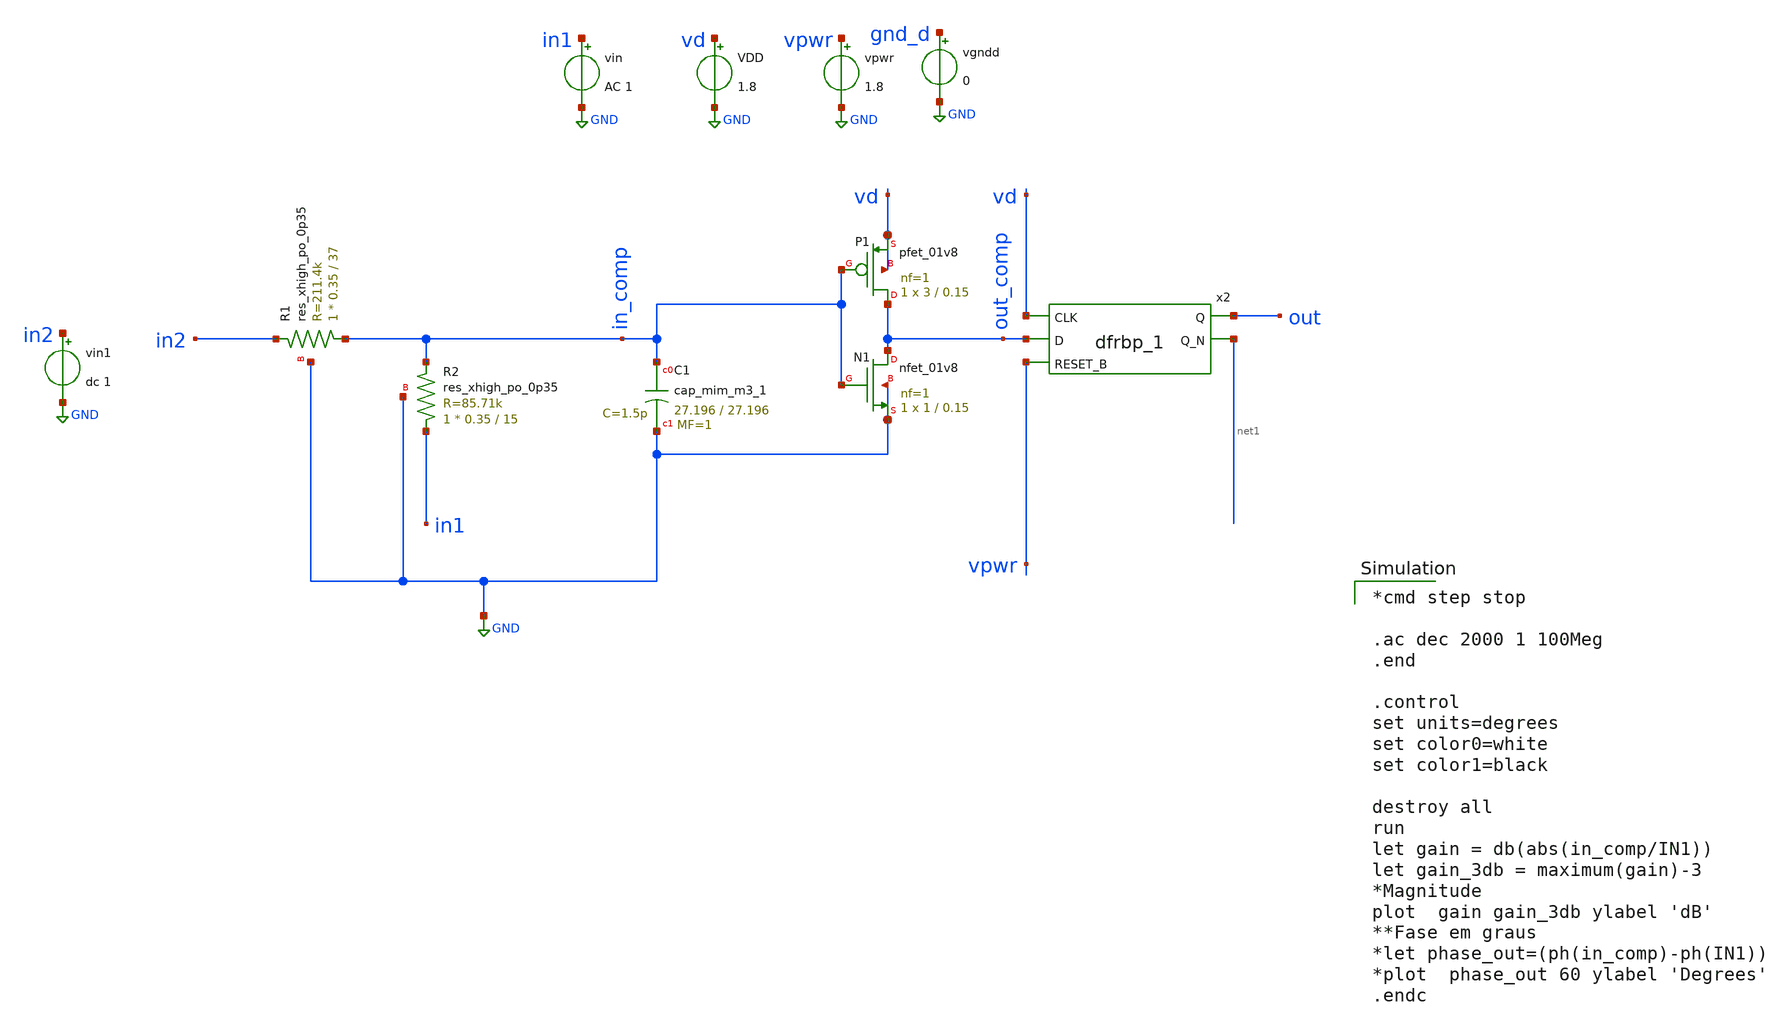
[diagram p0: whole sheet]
** sch_path: mag/sigma-delta_modulator/xschem/sum-integ_ac-tb.sch
* Copyright 2020 Stefan Frederik Schippers
* Licensed under the Apache License, Version 2.0 (the "License");
* you may not use this file except in compliance with the License.
* You may obtain a copy of the License at
* https://www.apache.org/licenses/LICENSE-2.0
* Unless required by applicable law or agreed to in writing, software
* distributed under the License is distributed on an "AS IS" BASIS,
* WITHOUT WARRANTIES OR CONDITIONS OF ANY KIND, either express or implied.
* See the License for the specific language governing permissions and
* limitations under the License.
**.subckt sum-integ_ac-tb
XC1 in_comp GND sky130_fd_pr__cap_mim_m3_1 W=27.196 L=27.196 MF=1 m=1
XR2 in1 in_comp GND sky130_fd_pr__res_xhigh_po_0p35 L=15 mult=1 m=1
x2 vd out_comp vpwr gnd_d gnd_d vpwr vpwr out net1 sky130_fd_sc_hd__dfrbp_1
XP1 out_comp in_comp vd vd sky130_fd_pr__pfet_01v8 L=0.15 W=3 nf=1 ad='int((nf+1)/2) * W/nf * 0.29' as='int((nf+2)/2) * W/nf * 0.29'
+ pd='2*int((nf+1)/2) * (W/nf + 0.29)' ps='2*int((nf+2)/2) * (W/nf + 0.29)' nrd='0.29 / W' nrs='0.29 / W'
+ sa=0 sb=0 sd=0 mult=1 m=1
XN1 out_comp in_comp GND GND sky130_fd_pr__nfet_01v8 L=0.15 W=1 nf=1 ad='int((nf+1)/2) * W/nf * 0.29'
+ as='int((nf+2)/2) * W/nf * 0.29' pd='2*int((nf+1)/2) * (W/nf + 0.29)' ps='2*int((nf+2)/2) * (W/nf + 0.29)'
+ nrd='0.29 / W' nrs='0.29 / W' sa=0 sb=0 sd=0 mult=1 m=1
XR1 in_comp in2 GND sky130_fd_pr__res_xhigh_po_0p35 L=37 mult=1 m=1
vin in1 GND AC 1
VDD vd GND 1.8
vpwr vpwr GND 1.8
vgndd gnd_d GND 0
vin1 in2 GND dc 1
**** begin user architecture code

*cmd step stop

.ac dec 2000 1 100Meg
.end

.control
set units=degrees
set color0=white
set color1=black

destroy all
run
let gain = db(abs(in_comp/IN1))
let gain_3db = maximum(gain)-3
*Magnitude
plot  gain gain_3db ylabel 'dB'
**Fase em graus
*let phase_out=(ph(in_comp)-ph(IN1))
*plot  phase_out 60 ylabel 'Degrees'
.endc

 .lib $::SKYWATER_MODELS/sky130.lib.spice tt
.include $::SKYWATER_STDCELLS/sky130_fd_sc_hd.spice

**** end user architecture code
**.ends
.GLOBAL GND
.end
